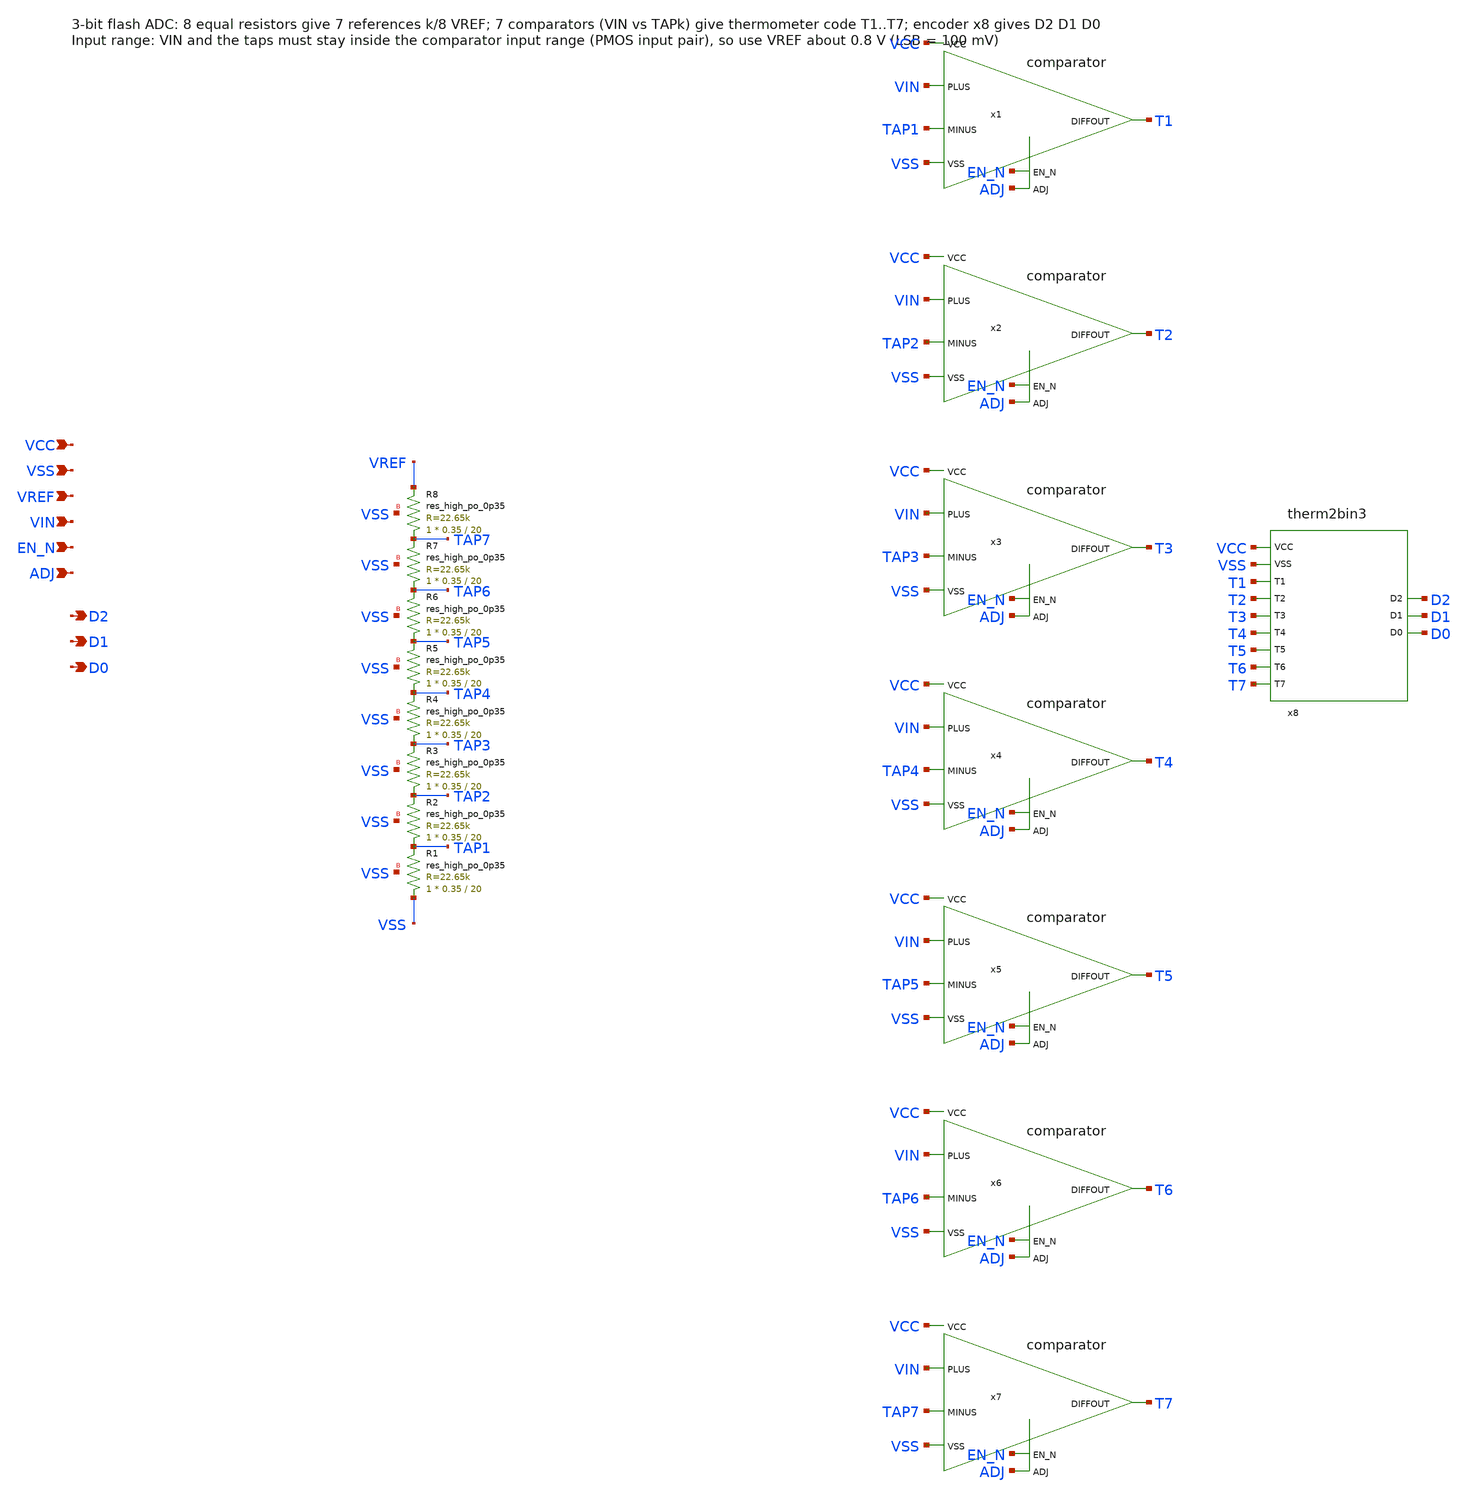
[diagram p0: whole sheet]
** sch_path: flash_adc3.sch
* comparator.sch:
* Copyright 2021 Stefan Frederik Schippers
* Licensed under the Apache License, Version 2.0 (the "License");
**.subckt flash_adc3 VCC VSS VREF VIN EN_N ADJ D2 D1 D0
*.ipin VCC
*.ipin VSS
*.ipin VREF
*.ipin VIN
*.ipin EN_N
*.ipin ADJ
*.opin D2
*.opin D1
*.opin D0
XR8 TAP7 VREF VSS sky130_fd_pr__res_high_po_0p35 L=20 mult=1 m=1
XR7 TAP6 TAP7 VSS sky130_fd_pr__res_high_po_0p35 L=20 mult=1 m=1
XR6 TAP5 TAP6 VSS sky130_fd_pr__res_high_po_0p35 L=20 mult=1 m=1
XR5 TAP4 TAP5 VSS sky130_fd_pr__res_high_po_0p35 L=20 mult=1 m=1
XR4 TAP3 TAP4 VSS sky130_fd_pr__res_high_po_0p35 L=20 mult=1 m=1
XR3 TAP2 TAP3 VSS sky130_fd_pr__res_high_po_0p35 L=20 mult=1 m=1
XR2 TAP1 TAP2 VSS sky130_fd_pr__res_high_po_0p35 L=20 mult=1 m=1
XR1 VSS TAP1 VSS sky130_fd_pr__res_high_po_0p35 L=20 mult=1 m=1
x1 VCC VSS EN_N TAP1 VIN ADJ T1 comparator
x2 VCC VSS EN_N TAP2 VIN ADJ T2 comparator
x3 VCC VSS EN_N TAP3 VIN ADJ T3 comparator
x4 VCC VSS EN_N TAP4 VIN ADJ T4 comparator
x5 VCC VSS EN_N TAP5 VIN ADJ T5 comparator
x6 VCC VSS EN_N TAP6 VIN ADJ T6 comparator
x7 VCC VSS EN_N TAP7 VIN ADJ T7 comparator
x8 VCC VSS T1 T2 T3 T4 T5 T6 T7 D2 D1 D0 therm2bin3
**.ends

* expanding   symbol:  /home/ttuser/Documents/ADCAnalogDesign/comparator.sym # of pins=7
** sym_path: comparator.sym
** sch_path: comparator.sch
.subckt comparator VCC VSS EN_N MINUS PLUS ADJ DIFFOUT
*.ipin VCC
*.ipin VSS
*.ipin EN_N
*.ipin MINUS
*.ipin PLUS
*.ipin ADJ
*.opin DIFFOUT
XM3 net1 EN_N VCC VCC sky130_fd_pr__pfet_01v8 L=8 W=1 nf=1 ad='int((nf+1)/2) * W/nf * 0.29' as='int((nf+2)/2) * W/nf * 0.29'
+ pd='2*int((nf+1)/2) * (W/nf + 0.29)' ps='2*int((nf+2)/2) * (W/nf + 0.29)' nrd='0.29 / W' nrs='0.29 / W'
+ sa=0 sb=0 sd=0 mult=1 m=1
XM7 Inhigh EN_N VCC VCC sky130_fd_pr__pfet_01v8 L=8 W=2 nf=1 ad='int((nf+1)/2) * W/nf * 0.29' as='int((nf+2)/2) * W/nf * 0.29'
+ pd='2*int((nf+1)/2) * (W/nf + 0.29)' ps='2*int((nf+2)/2) * (W/nf + 0.29)' nrd='0.29 / W' nrs='0.29 / W'
+ sa=0 sb=0 sd=0 mult=1 m=1
XM16 mirhigh EN_N VCC VCC sky130_fd_pr__pfet_01v8 L=0.15 W=5 nf=1 ad='int((nf+1)/2) * W/nf * 0.29' as='int((nf+2)/2) * W/nf * 0.29'
+ pd='2*int((nf+1)/2) * (W/nf + 0.29)' ps='2*int((nf+2)/2) * (W/nf + 0.29)' nrd='0.29 / W' nrs='0.29 / W'
+ sa=0 sb=0 sd=0 mult=1 m=1
XM4 G1 ADJ net1 VCC sky130_fd_pr__pfet_01v8_lvt L=1 W=1 nf=1 ad='int((nf+1)/2) * W/nf * 0.29' as='int((nf+2)/2) * W/nf * 0.29'
+ pd='2*int((nf+1)/2) * (W/nf + 0.29)' ps='2*int((nf+2)/2) * (W/nf + 0.29)' nrd='0.29 / W' nrs='0.29 / W'
+ sa=0 sb=0 sd=0 mult=1 m=1
XM5 G1 ADJ net2 VSS sky130_fd_pr__nfet_01v8_lvt L=1 W=0.5 nf=1 ad='int((nf+1)/2) * W/nf * 0.29' as='int((nf+2)/2) * W/nf * 0.29'
+ pd='2*int((nf+1)/2) * (W/nf + 0.29)' ps='2*int((nf+2)/2) * (W/nf + 0.29)' nrd='0.29 / W' nrs='0.29 / W'
+ sa=0 sb=0 sd=0 mult=1 m=1
XM6 net2 VCC VSS VSS sky130_fd_pr__nfet_01v8_lvt L=8 W=0.5 nf=1 ad='int((nf+1)/2) * W/nf * 0.29' as='int((nf+2)/2) * W/nf * 0.29'
+ pd='2*int((nf+1)/2) * (W/nf + 0.29)' ps='2*int((nf+2)/2) * (W/nf + 0.29)' nrd='0.29 / W' nrs='0.29 / W'
+ sa=0 sb=0 sd=0 mult=1 m=1
XM9 G1 MINUS Inhigh VCC sky130_fd_pr__pfet_01v8_lvt L=2 W=8 nf=1 ad='int((nf+1)/2) * W/nf * 0.29' as='int((nf+2)/2) * W/nf * 0.29'
+ pd='2*int((nf+1)/2) * (W/nf + 0.29)' ps='2*int((nf+2)/2) * (W/nf + 0.29)' nrd='0.29 / W' nrs='0.29 / W'
+ sa=0 sb=0 sd=0 mult=1 m=1
XM8 G2 PLUS Inhigh VCC sky130_fd_pr__pfet_01v8_lvt L=2 W=8 nf=1 ad='int((nf+1)/2) * W/nf * 0.29' as='int((nf+2)/2) * W/nf * 0.29'
+ pd='2*int((nf+1)/2) * (W/nf + 0.29)' ps='2*int((nf+2)/2) * (W/nf + 0.29)' nrd='0.29 / W' nrs='0.29 / W'
+ sa=0 sb=0 sd=0 mult=1 m=1
XM11 G2 G2 VSS VSS sky130_fd_pr__nfet_01v8_lvt L=4 W=2 nf=1 ad='int((nf+1)/2) * W/nf * 0.29' as='int((nf+2)/2) * W/nf * 0.29'
+ pd='2*int((nf+1)/2) * (W/nf + 0.29)' ps='2*int((nf+2)/2) * (W/nf + 0.29)' nrd='0.29 / W' nrs='0.29 / W'
+ sa=0 sb=0 sd=0 mult=1 m=1
XM10 G1 G1 VSS VSS sky130_fd_pr__nfet_01v8_lvt L=4 W=2 nf=1 ad='int((nf+1)/2) * W/nf * 0.29' as='int((nf+2)/2) * W/nf * 0.29'
+ pd='2*int((nf+1)/2) * (W/nf + 0.29)' ps='2*int((nf+2)/2) * (W/nf + 0.29)' nrd='0.29 / W' nrs='0.29 / W'
+ sa=0 sb=0 sd=0 mult=1 m=1
XM12 DIFFOUT G2 VSS VSS sky130_fd_pr__nfet_01v8_lvt L=4 W=2 nf=1 ad='int((nf+1)/2) * W/nf * 0.29' as='int((nf+2)/2) * W/nf * 0.29'
+ pd='2*int((nf+1)/2) * (W/nf + 0.29)' ps='2*int((nf+2)/2) * (W/nf + 0.29)' nrd='0.29 / W' nrs='0.29 / W'
+ sa=0 sb=0 sd=0 mult=1 m=1
XM13 DIFFOUT EN_N VSS VSS sky130_fd_pr__nfet_01v8_lvt L=0.15 W=1 nf=1 ad='int((nf+1)/2) * W/nf * 0.29'
+ as='int((nf+2)/2) * W/nf * 0.29' pd='2*int((nf+1)/2) * (W/nf + 0.29)' ps='2*int((nf+2)/2) * (W/nf + 0.29)'
+ nrd='0.29 / W' nrs='0.29 / W' sa=0 sb=0 sd=0 mult=1 m=1
XM17 pg2g G1 VSS VSS sky130_fd_pr__nfet_01v8_lvt L=4 W=2 nf=1 ad='int((nf+1)/2) * W/nf * 0.29' as='int((nf+2)/2) * W/nf * 0.29'
+ pd='2*int((nf+1)/2) * (W/nf + 0.29)' ps='2*int((nf+2)/2) * (W/nf + 0.29)' nrd='0.29 / W' nrs='0.29 / W'
+ sa=0 sb=0 sd=0 mult=1 m=1
XM15 pg2g pg2g mirhigh VCC sky130_fd_pr__pfet_01v8_lvt L=4 W=4 nf=1 ad='int((nf+1)/2) * W/nf * 0.29'
+ as='int((nf+2)/2) * W/nf * 0.29' pd='2*int((nf+1)/2) * (W/nf + 0.29)' ps='2*int((nf+2)/2) * (W/nf + 0.29)'
+ nrd='0.29 / W' nrs='0.29 / W' sa=0 sb=0 sd=0 mult=1 m=1
XM2 DIFFOUT pg2g mirhigh VCC sky130_fd_pr__pfet_01v8_lvt L=4 W=4 nf=1 ad='int((nf+1)/2) * W/nf * 0.29'
+ as='int((nf+2)/2) * W/nf * 0.29' pd='2*int((nf+1)/2) * (W/nf + 0.29)' ps='2*int((nf+2)/2) * (W/nf + 0.29)'
+ nrd='0.29 / W' nrs='0.29 / W' sa=0 sb=0 sd=0 mult=1 m=1
.ends


* expanding   symbol:  /home/ttuser/Documents/ADCAnalogDesign/therm2bin3.sym # of pins=12
** sym_path: therm2bin3.sym
** sch_path: therm2bin3.sch
.subckt therm2bin3 VCC VSS T1 T2 T3 T4 T5 T6 T7 D2 D1 D0
*.ipin VCC
*.ipin VSS
*.ipin T1
*.ipin T2
*.ipin T3
*.ipin T4
*.ipin T5
*.ipin T6
*.ipin T7
*.opin D2
*.opin D1
*.opin D0
XM1 T2B T2 VCC VCC sky130_fd_pr__pfet_01v8 L=0.15 W=2 nf=1 ad='int((nf+1)/2) * W/nf * 0.29' as='int((nf+2)/2) * W/nf * 0.29'
+ pd='2*int((nf+1)/2) * (W/nf + 0.29)' ps='2*int((nf+2)/2) * (W/nf + 0.29)' nrd='0.29 / W' nrs='0.29 / W'
+ sa=0 sb=0 sd=0 mult=1 m=1
XM2 T2B T2 VSS VSS sky130_fd_pr__nfet_01v8 L=0.15 W=1 nf=1 ad='int((nf+1)/2) * W/nf * 0.29' as='int((nf+2)/2) * W/nf * 0.29'
+ pd='2*int((nf+1)/2) * (W/nf + 0.29)' ps='2*int((nf+2)/2) * (W/nf + 0.29)' nrd='0.29 / W' nrs='0.29 / W'
+ sa=0 sb=0 sd=0 mult=1 m=1
XM3 T4B T4 VCC VCC sky130_fd_pr__pfet_01v8 L=0.15 W=2 nf=1 ad='int((nf+1)/2) * W/nf * 0.29' as='int((nf+2)/2) * W/nf * 0.29'
+ pd='2*int((nf+1)/2) * (W/nf + 0.29)' ps='2*int((nf+2)/2) * (W/nf + 0.29)' nrd='0.29 / W' nrs='0.29 / W'
+ sa=0 sb=0 sd=0 mult=1 m=1
XM4 T4B T4 VSS VSS sky130_fd_pr__nfet_01v8 L=0.15 W=1 nf=1 ad='int((nf+1)/2) * W/nf * 0.29' as='int((nf+2)/2) * W/nf * 0.29'
+ pd='2*int((nf+1)/2) * (W/nf + 0.29)' ps='2*int((nf+2)/2) * (W/nf + 0.29)' nrd='0.29 / W' nrs='0.29 / W'
+ sa=0 sb=0 sd=0 mult=1 m=1
XM5 T6B T6 VCC VCC sky130_fd_pr__pfet_01v8 L=0.15 W=2 nf=1 ad='int((nf+1)/2) * W/nf * 0.29' as='int((nf+2)/2) * W/nf * 0.29'
+ pd='2*int((nf+1)/2) * (W/nf + 0.29)' ps='2*int((nf+2)/2) * (W/nf + 0.29)' nrd='0.29 / W' nrs='0.29 / W'
+ sa=0 sb=0 sd=0 mult=1 m=1
XM6 T6B T6 VSS VSS sky130_fd_pr__nfet_01v8 L=0.15 W=1 nf=1 ad='int((nf+1)/2) * W/nf * 0.29' as='int((nf+2)/2) * W/nf * 0.29'
+ pd='2*int((nf+1)/2) * (W/nf + 0.29)' ps='2*int((nf+2)/2) * (W/nf + 0.29)' nrd='0.29 / W' nrs='0.29 / W'
+ sa=0 sb=0 sd=0 mult=1 m=1
XM7 T7B T7 VCC VCC sky130_fd_pr__pfet_01v8 L=0.15 W=2 nf=1 ad='int((nf+1)/2) * W/nf * 0.29' as='int((nf+2)/2) * W/nf * 0.29'
+ pd='2*int((nf+1)/2) * (W/nf + 0.29)' ps='2*int((nf+2)/2) * (W/nf + 0.29)' nrd='0.29 / W' nrs='0.29 / W'
+ sa=0 sb=0 sd=0 mult=1 m=1
XM8 T7B T7 VSS VSS sky130_fd_pr__nfet_01v8 L=0.15 W=1 nf=1 ad='int((nf+1)/2) * W/nf * 0.29' as='int((nf+2)/2) * W/nf * 0.29'
+ pd='2*int((nf+1)/2) * (W/nf + 0.29)' ps='2*int((nf+2)/2) * (W/nf + 0.29)' nrd='0.29 / W' nrs='0.29 / W'
+ sa=0 sb=0 sd=0 mult=1 m=1
XM9 D2 T4B VCC VCC sky130_fd_pr__pfet_01v8 L=0.15 W=2 nf=1 ad='int((nf+1)/2) * W/nf * 0.29' as='int((nf+2)/2) * W/nf * 0.29'
+ pd='2*int((nf+1)/2) * (W/nf + 0.29)' ps='2*int((nf+2)/2) * (W/nf + 0.29)' nrd='0.29 / W' nrs='0.29 / W'
+ sa=0 sb=0 sd=0 mult=1 m=1
XM10 D2 T4B VSS VSS sky130_fd_pr__nfet_01v8 L=0.15 W=1 nf=1 ad='int((nf+1)/2) * W/nf * 0.29' as='int((nf+2)/2) * W/nf * 0.29'
+ pd='2*int((nf+1)/2) * (W/nf + 0.29)' ps='2*int((nf+2)/2) * (W/nf + 0.29)' nrd='0.29 / W' nrs='0.29 / W'
+ sa=0 sb=0 sd=0 mult=1 m=1
XM11 N1 T1 VCC VCC sky130_fd_pr__pfet_01v8 L=0.15 W=2 nf=1 ad='int((nf+1)/2) * W/nf * 0.29' as='int((nf+2)/2) * W/nf * 0.29'
+ pd='2*int((nf+1)/2) * (W/nf + 0.29)' ps='2*int((nf+2)/2) * (W/nf + 0.29)' nrd='0.29 / W' nrs='0.29 / W'
+ sa=0 sb=0 sd=0 mult=1 m=1
XM12 N1 T2B VCC VCC sky130_fd_pr__pfet_01v8 L=0.15 W=2 nf=1 ad='int((nf+1)/2) * W/nf * 0.29' as='int((nf+2)/2) * W/nf * 0.29'
+ pd='2*int((nf+1)/2) * (W/nf + 0.29)' ps='2*int((nf+2)/2) * (W/nf + 0.29)' nrd='0.29 / W' nrs='0.29 / W'
+ sa=0 sb=0 sd=0 mult=1 m=1
XM13 N1 T1 N1_n1 VSS sky130_fd_pr__nfet_01v8 L=0.15 W=2 nf=1 ad='int((nf+1)/2) * W/nf * 0.29' as='int((nf+2)/2) * W/nf * 0.29'
+ pd='2*int((nf+1)/2) * (W/nf + 0.29)' ps='2*int((nf+2)/2) * (W/nf + 0.29)' nrd='0.29 / W' nrs='0.29 / W'
+ sa=0 sb=0 sd=0 mult=1 m=1
XM14 N1_n1 T2B VSS VSS sky130_fd_pr__nfet_01v8 L=0.15 W=2 nf=1 ad='int((nf+1)/2) * W/nf * 0.29' as='int((nf+2)/2) * W/nf * 0.29'
+ pd='2*int((nf+1)/2) * (W/nf + 0.29)' ps='2*int((nf+2)/2) * (W/nf + 0.29)' nrd='0.29 / W' nrs='0.29 / W'
+ sa=0 sb=0 sd=0 mult=1 m=1
XM15 N2 T3 VCC VCC sky130_fd_pr__pfet_01v8 L=0.15 W=2 nf=1 ad='int((nf+1)/2) * W/nf * 0.29' as='int((nf+2)/2) * W/nf * 0.29'
+ pd='2*int((nf+1)/2) * (W/nf + 0.29)' ps='2*int((nf+2)/2) * (W/nf + 0.29)' nrd='0.29 / W' nrs='0.29 / W'
+ sa=0 sb=0 sd=0 mult=1 m=1
XM16 N2 T4B VCC VCC sky130_fd_pr__pfet_01v8 L=0.15 W=2 nf=1 ad='int((nf+1)/2) * W/nf * 0.29' as='int((nf+2)/2) * W/nf * 0.29'
+ pd='2*int((nf+1)/2) * (W/nf + 0.29)' ps='2*int((nf+2)/2) * (W/nf + 0.29)' nrd='0.29 / W' nrs='0.29 / W'
+ sa=0 sb=0 sd=0 mult=1 m=1
XM17 N2 T3 N2_n1 VSS sky130_fd_pr__nfet_01v8 L=0.15 W=2 nf=1 ad='int((nf+1)/2) * W/nf * 0.29' as='int((nf+2)/2) * W/nf * 0.29'
+ pd='2*int((nf+1)/2) * (W/nf + 0.29)' ps='2*int((nf+2)/2) * (W/nf + 0.29)' nrd='0.29 / W' nrs='0.29 / W'
+ sa=0 sb=0 sd=0 mult=1 m=1
XM18 N2_n1 T4B VSS VSS sky130_fd_pr__nfet_01v8 L=0.15 W=2 nf=1 ad='int((nf+1)/2) * W/nf * 0.29' as='int((nf+2)/2) * W/nf * 0.29'
+ pd='2*int((nf+1)/2) * (W/nf + 0.29)' ps='2*int((nf+2)/2) * (W/nf + 0.29)' nrd='0.29 / W' nrs='0.29 / W'
+ sa=0 sb=0 sd=0 mult=1 m=1
XM19 N3 T5 VCC VCC sky130_fd_pr__pfet_01v8 L=0.15 W=2 nf=1 ad='int((nf+1)/2) * W/nf * 0.29' as='int((nf+2)/2) * W/nf * 0.29'
+ pd='2*int((nf+1)/2) * (W/nf + 0.29)' ps='2*int((nf+2)/2) * (W/nf + 0.29)' nrd='0.29 / W' nrs='0.29 / W'
+ sa=0 sb=0 sd=0 mult=1 m=1
XM20 N3 T6B VCC VCC sky130_fd_pr__pfet_01v8 L=0.15 W=2 nf=1 ad='int((nf+1)/2) * W/nf * 0.29' as='int((nf+2)/2) * W/nf * 0.29'
+ pd='2*int((nf+1)/2) * (W/nf + 0.29)' ps='2*int((nf+2)/2) * (W/nf + 0.29)' nrd='0.29 / W' nrs='0.29 / W'
+ sa=0 sb=0 sd=0 mult=1 m=1
XM21 N3 T5 N3_n1 VSS sky130_fd_pr__nfet_01v8 L=0.15 W=2 nf=1 ad='int((nf+1)/2) * W/nf * 0.29' as='int((nf+2)/2) * W/nf * 0.29'
+ pd='2*int((nf+1)/2) * (W/nf + 0.29)' ps='2*int((nf+2)/2) * (W/nf + 0.29)' nrd='0.29 / W' nrs='0.29 / W'
+ sa=0 sb=0 sd=0 mult=1 m=1
XM22 N3_n1 T6B VSS VSS sky130_fd_pr__nfet_01v8 L=0.15 W=2 nf=1 ad='int((nf+1)/2) * W/nf * 0.29' as='int((nf+2)/2) * W/nf * 0.29'
+ pd='2*int((nf+1)/2) * (W/nf + 0.29)' ps='2*int((nf+2)/2) * (W/nf + 0.29)' nrd='0.29 / W' nrs='0.29 / W'
+ sa=0 sb=0 sd=0 mult=1 m=1
XM23 N4 T2 VCC VCC sky130_fd_pr__pfet_01v8 L=0.15 W=2 nf=1 ad='int((nf+1)/2) * W/nf * 0.29' as='int((nf+2)/2) * W/nf * 0.29'
+ pd='2*int((nf+1)/2) * (W/nf + 0.29)' ps='2*int((nf+2)/2) * (W/nf + 0.29)' nrd='0.29 / W' nrs='0.29 / W'
+ sa=0 sb=0 sd=0 mult=1 m=1
XM24 N4 T4B VCC VCC sky130_fd_pr__pfet_01v8 L=0.15 W=2 nf=1 ad='int((nf+1)/2) * W/nf * 0.29' as='int((nf+2)/2) * W/nf * 0.29'
+ pd='2*int((nf+1)/2) * (W/nf + 0.29)' ps='2*int((nf+2)/2) * (W/nf + 0.29)' nrd='0.29 / W' nrs='0.29 / W'
+ sa=0 sb=0 sd=0 mult=1 m=1
XM25 N4 T2 N4_n1 VSS sky130_fd_pr__nfet_01v8 L=0.15 W=2 nf=1 ad='int((nf+1)/2) * W/nf * 0.29' as='int((nf+2)/2) * W/nf * 0.29'
+ pd='2*int((nf+1)/2) * (W/nf + 0.29)' ps='2*int((nf+2)/2) * (W/nf + 0.29)' nrd='0.29 / W' nrs='0.29 / W'
+ sa=0 sb=0 sd=0 mult=1 m=1
XM26 N4_n1 T4B VSS VSS sky130_fd_pr__nfet_01v8 L=0.15 W=2 nf=1 ad='int((nf+1)/2) * W/nf * 0.29' as='int((nf+2)/2) * W/nf * 0.29'
+ pd='2*int((nf+1)/2) * (W/nf + 0.29)' ps='2*int((nf+2)/2) * (W/nf + 0.29)' nrd='0.29 / W' nrs='0.29 / W'
+ sa=0 sb=0 sd=0 mult=1 m=1
XM27 D1 T6B VCC VCC sky130_fd_pr__pfet_01v8 L=0.15 W=2 nf=1 ad='int((nf+1)/2) * W/nf * 0.29' as='int((nf+2)/2) * W/nf * 0.29'
+ pd='2*int((nf+1)/2) * (W/nf + 0.29)' ps='2*int((nf+2)/2) * (W/nf + 0.29)' nrd='0.29 / W' nrs='0.29 / W'
+ sa=0 sb=0 sd=0 mult=1 m=1
XM28 D1 N4 VCC VCC sky130_fd_pr__pfet_01v8 L=0.15 W=2 nf=1 ad='int((nf+1)/2) * W/nf * 0.29' as='int((nf+2)/2) * W/nf * 0.29'
+ pd='2*int((nf+1)/2) * (W/nf + 0.29)' ps='2*int((nf+2)/2) * (W/nf + 0.29)' nrd='0.29 / W' nrs='0.29 / W'
+ sa=0 sb=0 sd=0 mult=1 m=1
XM29 D1 T6B D1_n1 VSS sky130_fd_pr__nfet_01v8 L=0.15 W=2 nf=1 ad='int((nf+1)/2) * W/nf * 0.29' as='int((nf+2)/2) * W/nf * 0.29'
+ pd='2*int((nf+1)/2) * (W/nf + 0.29)' ps='2*int((nf+2)/2) * (W/nf + 0.29)' nrd='0.29 / W' nrs='0.29 / W'
+ sa=0 sb=0 sd=0 mult=1 m=1
XM30 D1_n1 N4 VSS VSS sky130_fd_pr__nfet_01v8 L=0.15 W=2 nf=1 ad='int((nf+1)/2) * W/nf * 0.29' as='int((nf+2)/2) * W/nf * 0.29'
+ pd='2*int((nf+1)/2) * (W/nf + 0.29)' ps='2*int((nf+2)/2) * (W/nf + 0.29)' nrd='0.29 / W' nrs='0.29 / W'
+ sa=0 sb=0 sd=0 mult=1 m=1
XM31 D0 N1 VCC VCC sky130_fd_pr__pfet_01v8 L=0.15 W=2 nf=1 ad='int((nf+1)/2) * W/nf * 0.29' as='int((nf+2)/2) * W/nf * 0.29'
+ pd='2*int((nf+1)/2) * (W/nf + 0.29)' ps='2*int((nf+2)/2) * (W/nf + 0.29)' nrd='0.29 / W' nrs='0.29 / W'
+ sa=0 sb=0 sd=0 mult=1 m=1
XM32 D0 N2 VCC VCC sky130_fd_pr__pfet_01v8 L=0.15 W=2 nf=1 ad='int((nf+1)/2) * W/nf * 0.29' as='int((nf+2)/2) * W/nf * 0.29'
+ pd='2*int((nf+1)/2) * (W/nf + 0.29)' ps='2*int((nf+2)/2) * (W/nf + 0.29)' nrd='0.29 / W' nrs='0.29 / W'
+ sa=0 sb=0 sd=0 mult=1 m=1
XM33 D0 N3 VCC VCC sky130_fd_pr__pfet_01v8 L=0.15 W=2 nf=1 ad='int((nf+1)/2) * W/nf * 0.29' as='int((nf+2)/2) * W/nf * 0.29'
+ pd='2*int((nf+1)/2) * (W/nf + 0.29)' ps='2*int((nf+2)/2) * (W/nf + 0.29)' nrd='0.29 / W' nrs='0.29 / W'
+ sa=0 sb=0 sd=0 mult=1 m=1
XM34 D0 T7B VCC VCC sky130_fd_pr__pfet_01v8 L=0.15 W=2 nf=1 ad='int((nf+1)/2) * W/nf * 0.29' as='int((nf+2)/2) * W/nf * 0.29'
+ pd='2*int((nf+1)/2) * (W/nf + 0.29)' ps='2*int((nf+2)/2) * (W/nf + 0.29)' nrd='0.29 / W' nrs='0.29 / W'
+ sa=0 sb=0 sd=0 mult=1 m=1
XM35 D0 N1 D0_n1 VSS sky130_fd_pr__nfet_01v8 L=0.15 W=4 nf=1 ad='int((nf+1)/2) * W/nf * 0.29' as='int((nf+2)/2) * W/nf * 0.29'
+ pd='2*int((nf+1)/2) * (W/nf + 0.29)' ps='2*int((nf+2)/2) * (W/nf + 0.29)' nrd='0.29 / W' nrs='0.29 / W'
+ sa=0 sb=0 sd=0 mult=1 m=1
XM36 D0_n1 N2 D0_n2 VSS sky130_fd_pr__nfet_01v8 L=0.15 W=4 nf=1 ad='int((nf+1)/2) * W/nf * 0.29' as='int((nf+2)/2) * W/nf * 0.29'
+ pd='2*int((nf+1)/2) * (W/nf + 0.29)' ps='2*int((nf+2)/2) * (W/nf + 0.29)' nrd='0.29 / W' nrs='0.29 / W'
+ sa=0 sb=0 sd=0 mult=1 m=1
XM37 D0_n2 N3 D0_n3 VSS sky130_fd_pr__nfet_01v8 L=0.15 W=4 nf=1 ad='int((nf+1)/2) * W/nf * 0.29' as='int((nf+2)/2) * W/nf * 0.29'
+ pd='2*int((nf+1)/2) * (W/nf + 0.29)' ps='2*int((nf+2)/2) * (W/nf + 0.29)' nrd='0.29 / W' nrs='0.29 / W'
+ sa=0 sb=0 sd=0 mult=1 m=1
XM38 D0_n3 T7B VSS VSS sky130_fd_pr__nfet_01v8 L=0.15 W=4 nf=1 ad='int((nf+1)/2) * W/nf * 0.29' as='int((nf+2)/2) * W/nf * 0.29'
+ pd='2*int((nf+1)/2) * (W/nf + 0.29)' ps='2*int((nf+2)/2) * (W/nf + 0.29)' nrd='0.29 / W' nrs='0.29 / W'
+ sa=0 sb=0 sd=0 mult=1 m=1
.ends

.end
